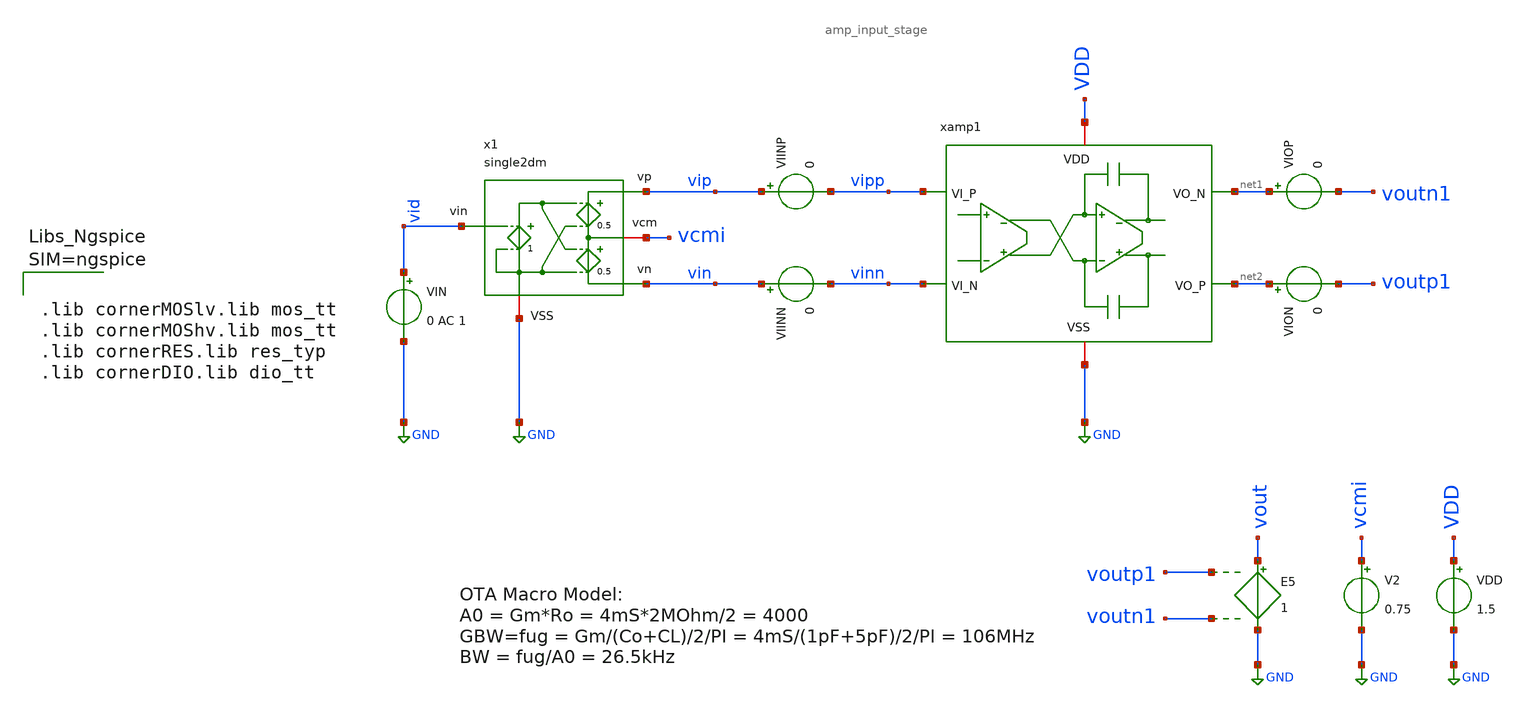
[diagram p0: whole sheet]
** sch_path: macros/filter_cmos5l/testbenches/xschem/ota_input_stage_tb.sch
**.subckt ota_input_stage_tb
V2 vcmi GND 0.75
VIN vid GND 0 AC 1
VIINP vip vipp 0
VIINN vin vinn 0
E5 vout GND voutp1 voutn1 1
VIOP net1 voutn1 0
VION net2 voutp1 0
x1 vip vid vcmi GND vin single2dm
xamp1 VDD vinn vipp net2 net1 GND amp_input_stage
VDD VDD GND 1.5
**** begin user architecture code


.include ota_input_stage_tb.save
.options savecurrents
.options method=gear reltol=.005
.options sparse
.control
save all

let f_sig = 100
let f_min = 10
let f_max = 1000Meg
let f_stop = 5Meg
let tper_sig = 1/f_sig
let tfr_sig = tper_sig/2
let Adc = 4000
let v_step_o = 0.75
let v_step_i = v_step_o/Adc

let t_rf = 0.1u
let t_step = 50u
let t_delay = 0
let t_per = 2*t_step

let tstep = 0.1*t_rf
let tstop = 2*t_per
let tstart = t_delay

alter @VIN[PULSE] = [ 0 $&v_step_i $&t_delay $&t_rf $&t_rf $&t_step $&t_per 0 ]

set wr_singlescale
set wr_vecnames
option numdgt=3


** Main Simulations
	op
	ac dec 100 $&const.f_min $&const.f_max
	tran $&tstep $&tstop $&tstart

	setplot ac1
	let A = v(vout)/v(vid)

	let Amag_dB = vdb(A)
	settype decibel Amag_dB
	let Aarg = 180/PI*cphase(A)

	let fdc = const.f_min+1
	meas ac Adc find Amag_dB when frequency = fdc
	let Amag_fc = Adc-3
	meas ac fc find frequency when Amag_dB = Amag_fc
	meas ac Amax max Amag_dB
	meas ac fug find frequency when Amag_dB=0

	let Adc_lin = 10^(Adc/20)
	let GBW = Adc_lin*fc
	print Adc_lin
	print GBW

	plot Amag_dB Aarg ylabel 'Magnitude, Phase'

	setplot tran1
	let vid = v(vid)
	let iop = viop#branch
	let ion = vion#branch
	let vcmo = (voutp1+voutn1)/2

	*plot iop ion
	plot vid vout vcmo
	plot v(vip) v(vin) v(voutp1) v(voutn1) vcmo


alter @VIN[DC] = 0
op

remzerovec
write ota_input_stage_tb.raw
.endc




.lib cornerMOSlv.lib mos_tt
.lib cornerMOShv.lib mos_tt
.lib cornerRES.lib res_typ
.lib cornerDIO.lib dio_tt



**** end user architecture code
**.ends

* expanding   symbol:  single2dm.sym # of pins=5
** sym_path: single2dm.sym
** sch_path: single2dm.sch
.subckt single2dm vp vin vcm VSS vn
*.ipin vin
*.opin vn
*.iopin vcm
*.opin vp
*.iopin VSS
E3 vcm vn net1 VSS 0.5
E2 vp vcm net1 VSS 0.5
E1 net1 VSS vin VSS 1
.ends


* expanding   symbol:  amp_input_stage.sym # of pins=6
** sym_path: macros/filter_cmos5l/schematic/xschem/amp_input_stage.sym
** sch_path: macros/filter_cmos5l/schematic/xschem/amp_input_stage.sch
.subckt amp_input_stage VDD VI_N VI_P VO_P VO_N VSS
*.iopin VSS
*.iopin VDD
*.ipin VI_P
*.ipin VI_N
*.opin VO_N
*.opin VO_P
XM12 VO_N vfb1 VSS VSS sg13_lv_nmos w=4u l=0.5u ng=8 m=1 mm_ok=1
XM13 VO_P vfb1 VSS VSS sg13_lv_nmos w=4u l=0.5u ng=8 m=1 mm_ok=1
XM18 VO_N VI_P viref1 viref1 sg13_lv_pmos w=48.5u l=0.13u ng=10 m=1 mm_ok=1
XM19 VO_P VI_N viref1 viref1 sg13_lv_pmos w=48.5u l=0.13u ng=10 m=1 mm_ok=1
I0 VDD viref1 520u
xr1 vfb1 VO_N VO_P VSS rstring_cm
.ends


* expanding   symbol:  rstring_cm.sym # of pins=4
** sym_path: rstring_cm.sym
** sch_path: rstring_cm.sch
.subckt rstring_cm VR_M VR_N VR_P VSS
*.iopin VSS
*.ipin VR_P
*.ipin VR_N
*.opin VR_M
R1 VR_P VR_M 1Meg m=1
R4 VR_M VR_N 1Meg m=1
.ends

.GLOBAL GND
.end
